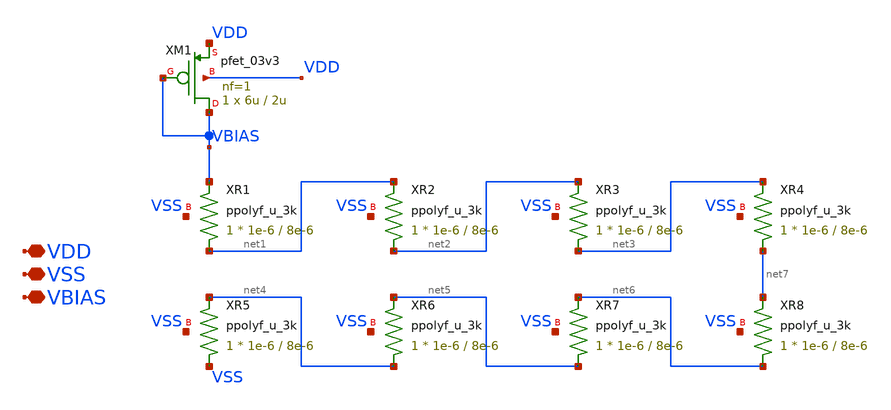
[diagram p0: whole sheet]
** sch_path: designs/libs/OTA/pbias-gen (1).sch
**.subckt pbias-gen (1) VDD VSS VBIAS
*.iopin VDD
*.iopin VSS
*.iopin VBIAS
XM1 VBIAS VBIAS VDD VDD pfet_03v3 L=2u W=6u nf=1 ad='int((nf+1)/2) * W/nf * 0.18u' as='int((nf+2)/2) * W/nf * 0.18u'
+ pd='2*int((nf+1)/2) * (W/nf + 0.18u)' ps='2*int((nf+2)/2) * (W/nf + 0.18u)' nrd='0.18u / W' nrs='0.18u / W'
+ sa=0 sb=0 sd=0 m=1
XR1 net1 VBIAS VSS ppolyf_u_3k r_width=1e-6 r_length=8e-6 m=1
XR2 net2 net1 VSS ppolyf_u_3k r_width=1e-6 r_length=8e-6 m=1
XR3 net3 net2 VSS ppolyf_u_3k r_width=1e-6 r_length=8e-6 m=1
XR4 net7 net3 VSS ppolyf_u_3k r_width=1e-6 r_length=8e-6 m=1
XR5 VSS net4 VSS ppolyf_u_3k r_width=1e-6 r_length=8e-6 m=1
XR6 net4 net5 VSS ppolyf_u_3k r_width=1e-6 r_length=8e-6 m=1
XR7 net5 net6 VSS ppolyf_u_3k r_width=1e-6 r_length=8e-6 m=1
XR8 net6 net7 VSS ppolyf_u_3k r_width=1e-6 r_length=8e-6 m=1
**.ends
.end
